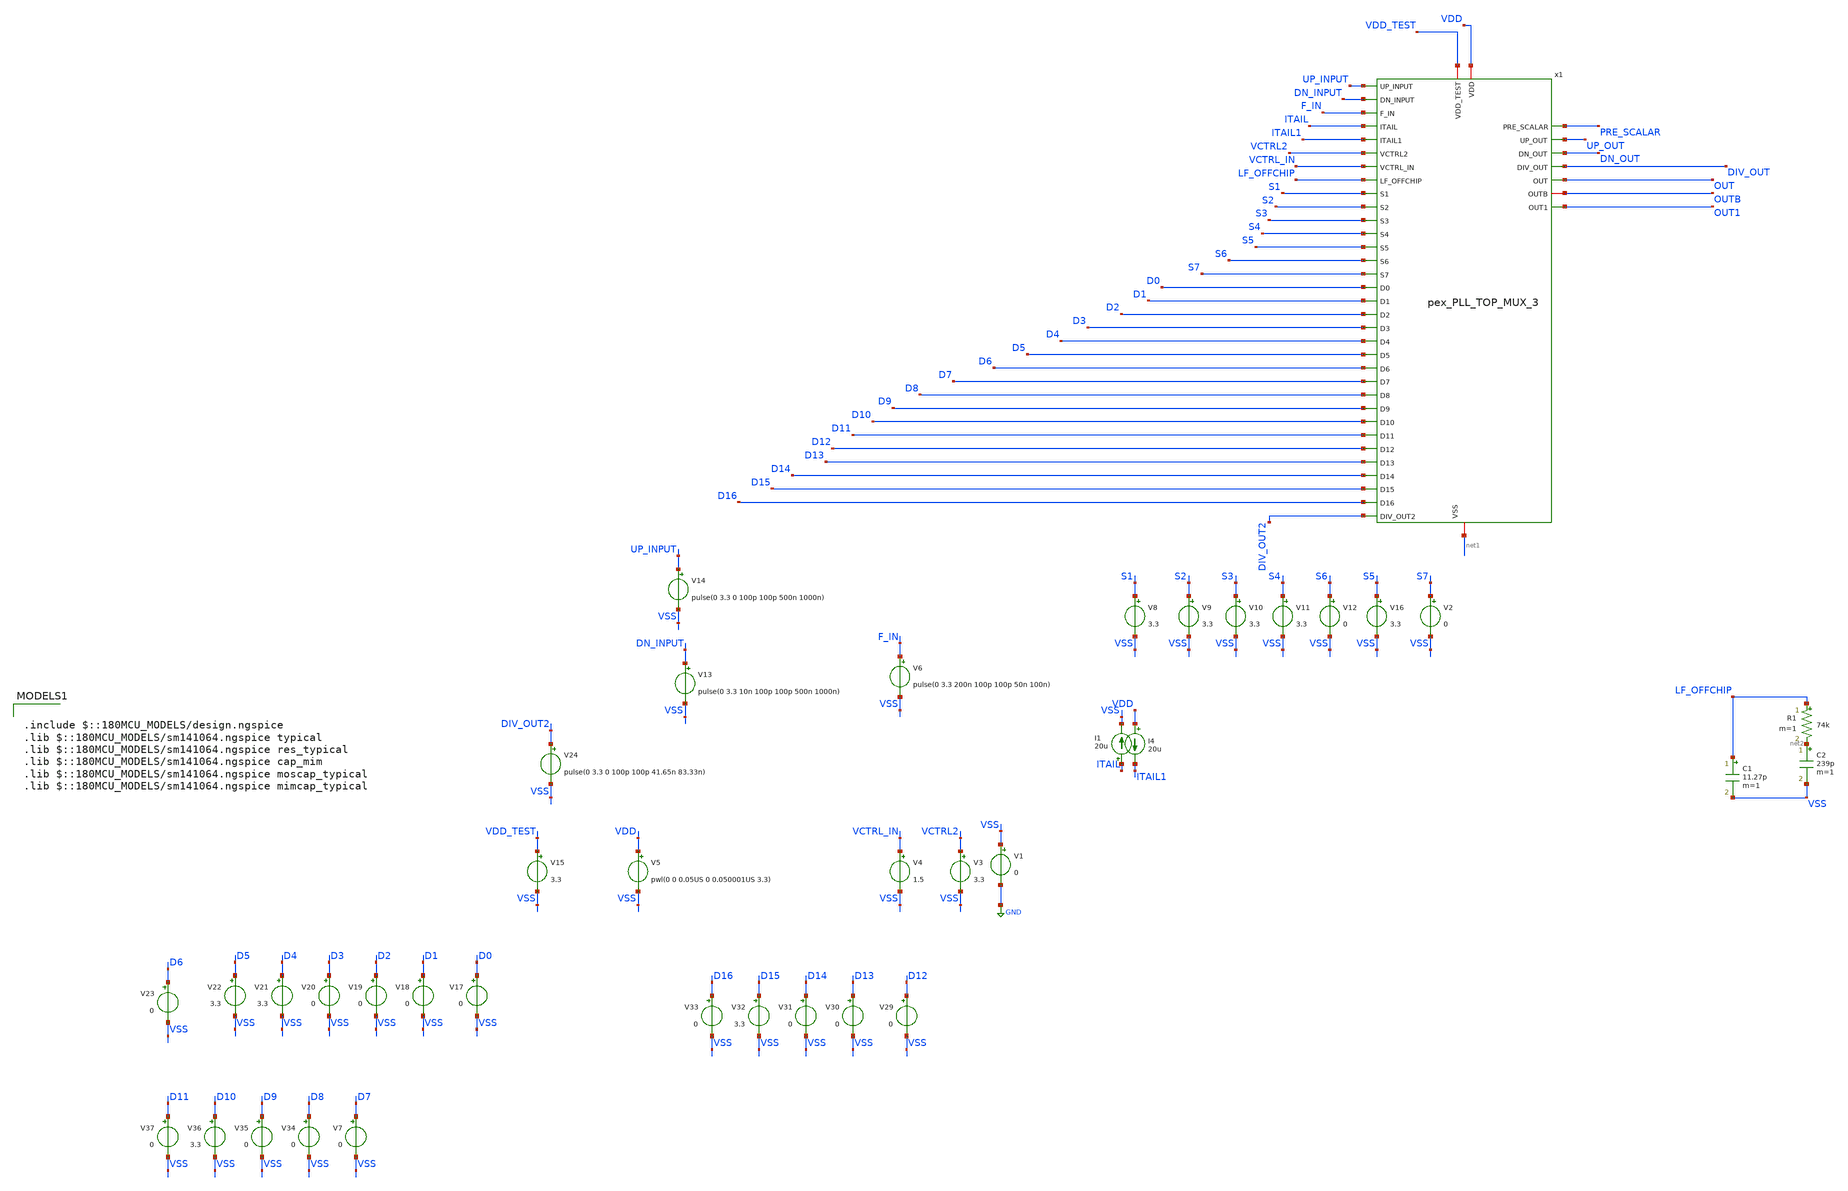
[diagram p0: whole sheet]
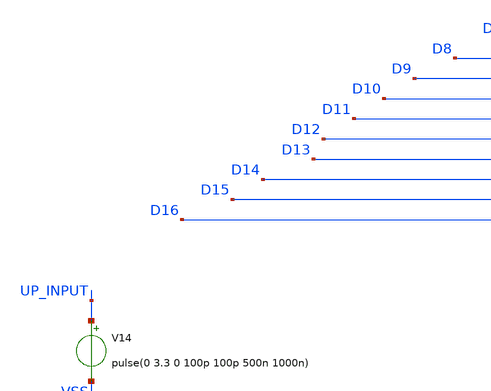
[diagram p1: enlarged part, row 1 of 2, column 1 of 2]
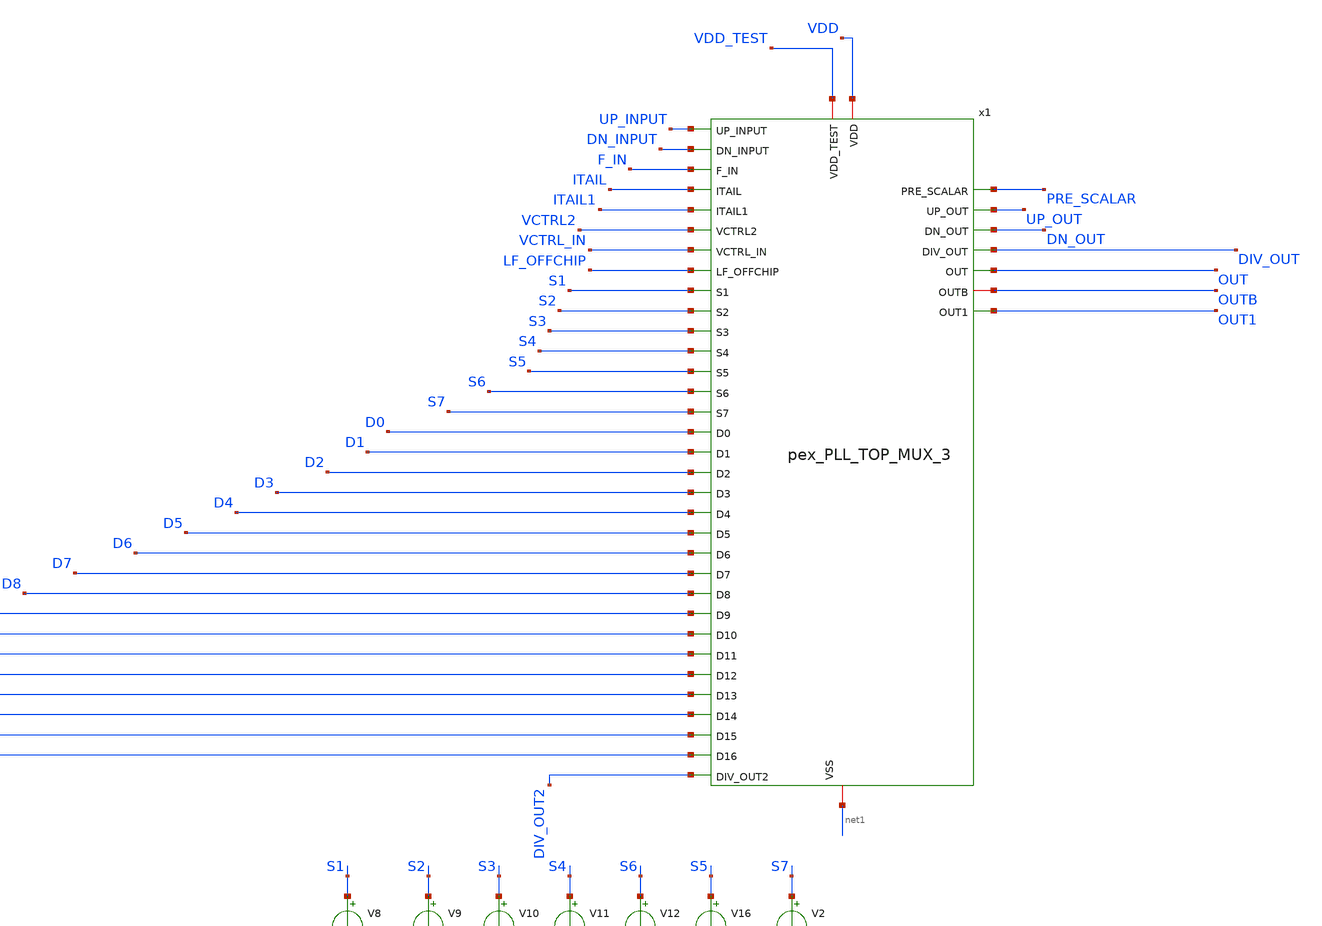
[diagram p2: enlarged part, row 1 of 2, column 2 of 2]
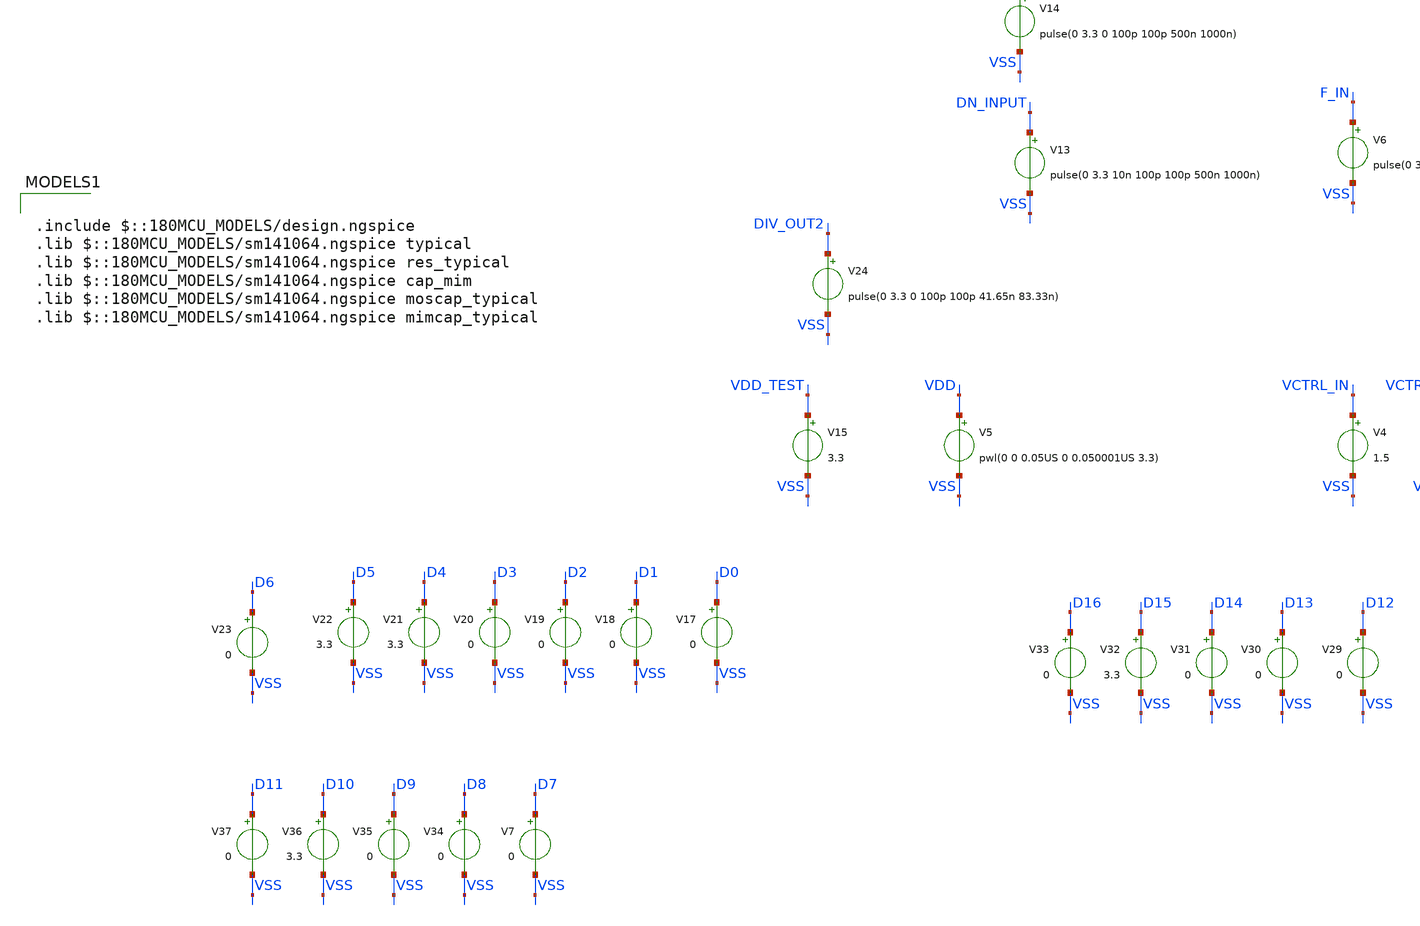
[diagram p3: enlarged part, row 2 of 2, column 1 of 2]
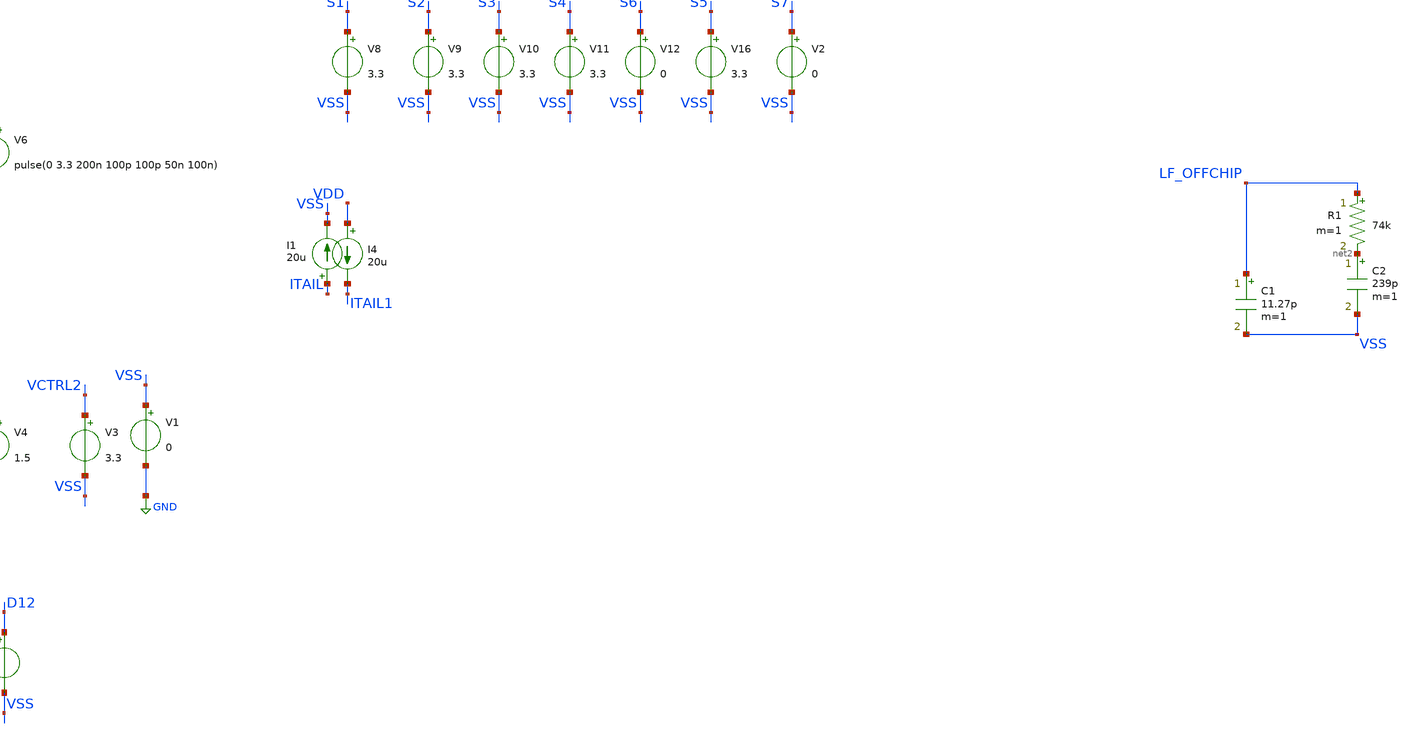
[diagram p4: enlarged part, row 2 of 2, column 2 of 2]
** sch_path: Clock_Generator_PAKISTAN_06/Xschem/TB_TOP_MUX_F.sch
**.subckt TB_TOP_MUX_F
V1 VSS GND 0
V3 VCTRL2 VSS 3.3
V4 VCTRL_IN VSS 1.5
V6 F_IN VSS pulse(0 3.3 200n 100p 100p 50n 100n)
I1 ITAIL VSS 20u
I4 VDD ITAIL1 20u
V8 S1 VSS 3.3
V9 S2 VSS 3.3
V10 S3 VSS 3.3
V11 S4 VSS 3.3
V12 S6 VSS 0
V13 DN_INPUT VSS pulse(0 3.3 10n 100p 100p 500n 1000n)
V14 UP_INPUT VSS pulse(0 3.3 0 100p 100p 500n 1000n)
V15 VDD_TEST VSS 3.3
C1 LF_OFFCHIP VSS 11.27p m=1
R1 LF_OFFCHIP net2 74k m=1
C2 net2 VSS 239p m=1
V16 S5 VSS 3.3
V17 D0 VSS 0
V18 D1 VSS 0
V19 D2 VSS 0
V20 D3 VSS 0
V21 D4 VSS 3.3
V22 D5 VSS 3.3
V23 D6 VSS 0
V29 D12 VSS 0
V30 D13 VSS 0
V31 D14 VSS 0
V32 D15 VSS 3.3
V33 D16 VSS 0
V2 S7 VSS 0
V5 VDD VSS pwl(0 0 0.05US 0 0.050001US 3.3)
V7 D7 VSS 0
V34 D8 VSS 0
V35 D9 VSS 0
V36 D10 VSS 3.3
V37 D11 VSS 0
V24 DIV_OUT2 VSS pulse(0 3.3 0 100p 100p 41.65n 83.33n)
x1 VDD_TEST D12 D0 UP_INPUT VDD D13 D1 DN_INPUT net1 D14 D2 PRE_SCALAR UP_OUT D15 D3 F_IN DN_OUT D16
+ D4 ITAIL DIV_OUT D5 ITAIL1 S1 D6 VCTRL_IN S6 D7 VCTRL2 S2 D8 OUT S3 S4 OUTB D9 S5 D10 LF_OFFCHIP S7
+ D11 OUT1 DIV_OUT2 pex_PLL_TOP_MUX_3
**** begin user architecture code


.include pex_PLL_TOP_MUX_3.spice
*.include pex_7b_divider_magic.spice
*.include pex_PLL_TOP_MUX_2.spice
*.include Tappered-Buffer_1_pex.spice
*.option RSHUNT=1e18
**.option ABSTOL=1e-12
**.option VNTOL=1e-12
**.option CHGTOL=1e-14
**.option RELTOL=1e-5
.option gmin=1e-12
**.option trtol=1
**.OPTION ITL4=500
.control
save all
save x1.vco_dff_c_0.vctrl.t19  x1.pre_scalar.n0  pre_scalar  x1.vss.t6260  x1.vdd.n7823
+  x1.vctrl_in.t6  x1.vctrl2.t62  x1.vco_dff_c_0.vco_c_0.outb.t53  x1.vco_dff_c_0.vco_c_0.inv_2_5.in.n34
+  x1.vco_dff_c_0.vco_c_0.inv_2_3.out.n2  x1.vco_dff_c_0.vco_c_0.inv_2_2.in.n30  x1.vco_dff_c_0.vco_c_0.inv_2_0.in.n51
+  x1.vco_dff_c_0.outb.t31  x1.vco_dff_c_0.out.t10  x1.up_out.t60  x1.up_input.n12  x1.up1.n10  x1.up.n28  x1.a_mux_6.in1.n194
+  x1.a_mux_5.in1.t163  x1.a_mux_2.out.n14  x1.a_mux_1.out  x1.a_mux_6.out
+  x1.7b_divider_magic_2.p2_gen_magic_0.dff_magic_0.tg_magic_3.out  x1.7b_divider_magic_2.p2_gen_magic_0.dff_magic_0.tg_magic_3.clk
+  x1.7b_divider_magic_2.p2_gen_magic_0.dff_magic_0.tg_magic_2.in.n10  x1.7b_divider_magic_2.p2.t16  x1.7b_divider_magic_2.out1.t8
+  x1.7b_divider_magic_2.divide_by_2_1.tg_magic_3.out  x1.7b_divider_magic_2.divide_by_2_1.tg_magic_3.clk
+  x1.7b_divider_magic_1.p2_gen_magic_0.dff_magic_0.tg_magic_1.in.n19  x1.7b_divider_magic_1.ld  x1.7b_divider_magic_1.divide_by_2_1.tg_magic_2.in.n14
+  x1.7b_divider_magic_1.divide_by_2_0.tg_magic_3.out  x1.7b_divider_magic_1.divide_by_2_0.tg_magic_3.in  x1.7b_divider_magic_0.out1
+  x1.7b_divider_magic_0.ld.n38  x1.vctrl_obv  d11  d10  d9  d8  d7  d6  d5  d4  d3  d2  d1  d0  out1  out  net1  lf_offchip
+  itail1  itail  f_in  dn_out  dn_input  div_out  d16  d15  d14  d13  d12
*set ngbehavior=hsa
*set ng_nomodcheck
tran 500n 3u
set appendwrite
write TB_TOP_MUX_F.raw
.endc



.include $::180MCU_MODELS/design.ngspice
.lib $::180MCU_MODELS/sm141064.ngspice typical
.lib $::180MCU_MODELS/sm141064.ngspice res_typical
.lib $::180MCU_MODELS/sm141064.ngspice cap_mim
.lib $::180MCU_MODELS/sm141064.ngspice moscap_typical
.lib $::180MCU_MODELS/sm141064.ngspice mimcap_typical

**** end user architecture code
**.ends
.GLOBAL GND
.end
